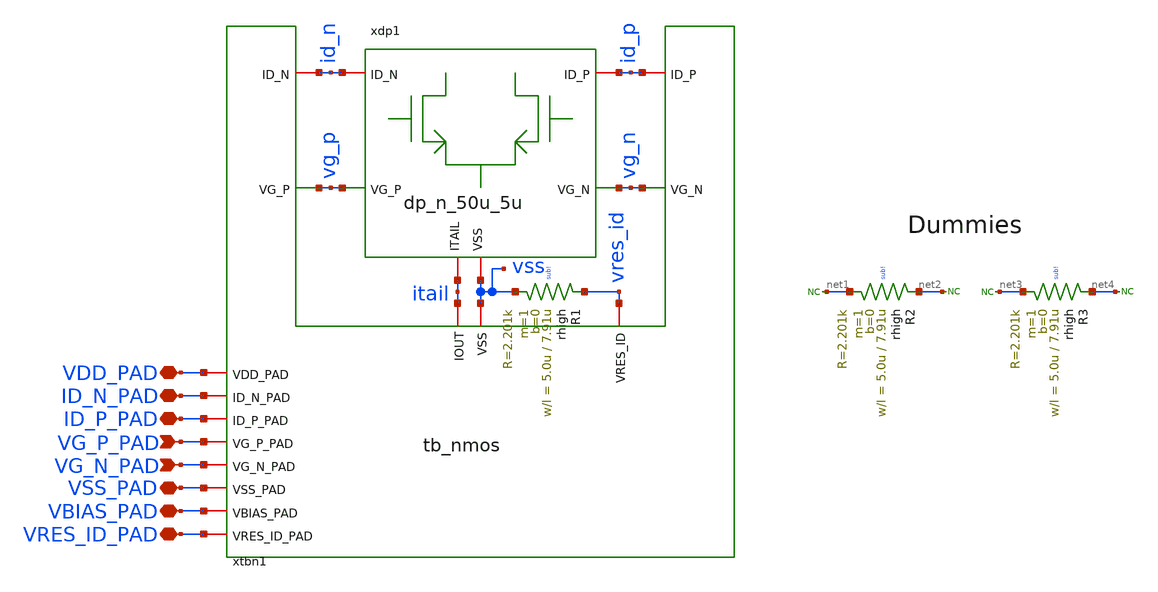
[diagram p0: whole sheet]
** sch_path: JKU_TC1/design_data/sfl-test-cells/xschem/testcells/tc_n_50u_5u.sch
**.subckt tc_n_50u_5u VDD_PAD ID_N_PAD ID_P_PAD VSS_PAD VBIAS_PAD VRES_ID_PAD VG_N_PAD VG_P_PAD
*.iopin VDD_PAD
*.iopin ID_N_PAD
*.iopin ID_P_PAD
*.iopin VSS_PAD
*.iopin VBIAS_PAD
*.iopin VRES_ID_PAD
*.ipin VG_N_PAD
*.ipin VG_P_PAD
xtbn1 id_n id_p vg_p vg_n vres_id itail VDD_PAD ID_N_PAD ID_P_PAD VG_P_PAD VG_N_PAD VSS_PAD
+ VBIAS_PAD VRES_ID_PAD vss tb_nmos
xdp1 id_n id_p vg_p vg_n itail vss dp_n_50u_5u
XR1 vres_id vss sub! rhigh w=5.0u l=7.91u m=1 b=0 mm_ok=1
XR2 net2 net1 sub! rhigh w=5.0u l=7.91u m=1 b=0 mm_ok=1
* noconn #net1
* noconn #net2
XR3 net4 net3 sub! rhigh w=5.0u l=7.91u m=1 b=0 mm_ok=1
* noconn #net3
* noconn #net4
**.ends

* expanding   symbol:  testcells/tb_nmos.sym # of pins=15
** sym_path: JKU_TC1/design_data/sfl-test-cells/xschem/testcells/tb_nmos.sym
** sch_path: JKU_TC1/design_data/sfl-test-cells/xschem/testcells/tb_nmos.sch
.subckt tb_nmos ID_N ID_P VG_P VG_N VRES_ID IOUT VDD_PAD ID_N_PAD ID_P_PAD VG_P_PAD VG_N_PAD VSS_PAD
+ VBIAS_PAD VRES_ID_PAD VSS
*.iopin VDD_PAD
*.iopin ID_N_PAD
*.iopin ID_P_PAD
*.iopin VG_P_PAD
*.iopin VG_N_PAD
*.iopin VSS_PAD
*.iopin VBIAS_PAD
*.iopin VRES_ID_PAD
*.iopin VSS
*.iopin IOUT
*.iopin VRES_ID
*.iopin ID_N
*.iopin ID_P
*.ipin VG_P
*.ipin VG_N
xpads1 VSS_PAD VDD_PAD VG_P_PAD VG_N_PAD ID_N_PAD ID_P_PAD VBIAS_PAD VRES_ID_PAD vdd VSS VG_N VG_P
+ VRES_ID ID_P vbias VSS ID_N vdd pad_ana_x8
xtail1 IOUT vbias VSS tail_src_n
.ends


* expanding   symbol:  diffpairs/dp_n_50u_5u.sym # of pins=6
** sym_path: JKU_TC1/design_data/sfl-test-cells/xschem/diffpairs/dp_n_50u_5u.sym
** sch_path: JKU_TC1/design_data/sfl-test-cells/xschem/diffpairs/dp_n_50u_5u.sch
.subckt dp_n_50u_5u ID_N ID_P VG_P VG_N ITAIL VSS
*.ipin VG_P
*.ipin VG_N
*.iopin VSS
*.iopin ITAIL
*.iopin ID_N
*.iopin ID_P
XM1 ITAIL VG_P ID_N VSS sg13_lv_nmos w=10.0u l=5.0u ng=4 m=5 mm_ok=1
XM2 ITAIL VG_N ID_P VSS sg13_lv_nmos w=10.0u l=5.0u ng=4 m=5 mm_ok=1
XM3 VSS VSS ITAIL VSS sg13_lv_nmos w=5.0u l=5.0u ng=2 m=5 mm_ok=1
XM4 VSS VSS VSS VSS sg13_lv_nmos w=50.0u l=5.0u ng=20 m=1 mm_ok=1
.ends


* expanding   symbol:  pads/pad_ana_x8.sym # of pins=18
** sym_path: JKU_TC1/design_data/xschem/pads/pad_ana_x8.sym
** sch_path: JKU_TC1/design_data/xschem/pads/pad_ana_x8.sch
.subckt pad_ana_x8 PAD6 PAD1 PAD4 PAD5 PAD2 PAD3 PAD7 PAD8 VDD VSS ANA5 ANA4 ANA8 ANA3 ANA7 ANA6
+ ANA2 ANA1
*.iopin VDD
*.iopin VSS
*.iopin ANA1
*.iopin ANA2
*.iopin ANA3
*.iopin ANA4
*.iopin ANA5
*.iopin ANA6
*.iopin ANA7
*.iopin ANA8
*.iopin PAD1
*.iopin PAD2
*.iopin PAD3
*.iopin PAD4
*.iopin PAD5
*.iopin PAD6
*.iopin PAD7
*.iopin PAD8
xpad1 VDD PAD1 ANA1 VSS pad_ana
xpad2 VDD PAD2 ANA2 VSS pad_ana
xpad3 VDD PAD3 ANA3 VSS pad_ana
xpad4 VDD PAD4 ANA4 VSS pad_ana
xpad5 VDD PAD5 ANA5 VSS pad_ana
xpad6 VDD PAD6 ANA6 VSS pad_ana
xpad7 VDD PAD7 ANA7 VSS pad_ana
xpad8 VDD PAD8 ANA8 VSS pad_ana
.ends


* expanding   symbol:  tailsrcs/tail_src_n.sym # of pins=3
** sym_path: JKU_TC1/design_data/sfl-test-cells/xschem/tailsrcs/tail_src_n.sym
** sch_path: JKU_TC1/design_data/sfl-test-cells/xschem/tailsrcs/tail_src_n.sch
.subckt tail_src_n IOUT VBIAS VSS
*.ipin VBIAS
*.iopin VSS
*.iopin IOUT
XM1 VSS VBIAS IOUT VSS sg13_lv_nmos w=160u l=10u ng=20 m=5 mm_ok=1
XM2 VSS VBIAS VSS VSS sg13_lv_nmos w=8u l=10u ng=1 m=10 mm_ok=1
XM3 VSS VBIAS VSS VSS sg13_lv_nmos w=176u l=10u ng=22 m=2 mm_ok=1
.ends


* expanding   symbol:  pads/pad_ana.sym # of pins=4
** sym_path: JKU_TC1/design_data/xschem/pads/pad_ana.sym
** sch_path: JKU_TC1/design_data/xschem/pads/pad_ana.sch
.subckt pad_ana VDD PAD ANA VSS
*.iopin VSS
*.iopin PAD
*.iopin VDD
*.iopin ANA
XC1 VDD PAD cparasitic C=20f
XC2 PAD VSS cparasitic C=20f
R1 PAD ANA 1e-6 m=1
R2 PAD ANA 1e-6 m=1
xesd1 VDD PAD VSS pad_diodes
.ends


* expanding   symbol:  pads/pad_diodes.sym # of pins=3
** sym_path: JKU_TC1/design_data/xschem/pads/pad_diodes.sym
** sch_path: JKU_TC1/design_data/xschem/pads/pad_diodes.sch
.subckt pad_diodes VDD PAD VSS
*.iopin VDD
*.iopin VSS
*.iopin PAD
XXD1 PAD VDD dantenna l=780n w=780n
XXD2 VSS PAD dantenna l=780n w=780n
.ends

.end
